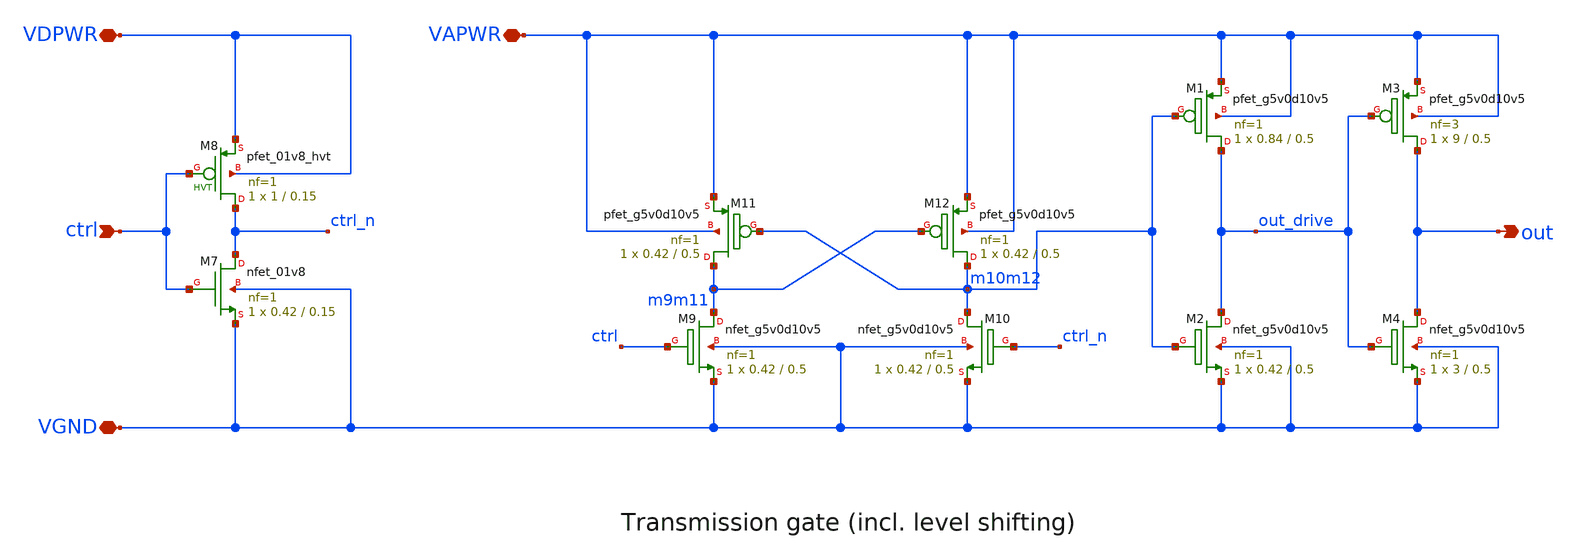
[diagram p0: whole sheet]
** sch_path: xschem/dac_drive.sch
**.subckt dac_drive ctrl VGND VDPWR VAPWR out
*.ipin ctrl
*.iopin VGND
*.iopin VDPWR
*.iopin VAPWR
*.opin out
XM8 ctrl_n ctrl VDPWR VDPWR sky130_fd_pr__pfet_01v8_hvt L=0.15 W=1 nf=1 ad='int((nf+1)/2) * W/nf * 0.29'
+ as='int((nf+2)/2) * W/nf * 0.29' pd='2*int((nf+1)/2) * (W/nf + 0.29)' ps='2*int((nf+2)/2) * (W/nf + 0.29)'
+ nrd='0.29 / W' nrs='0.29 / W' sa=0 sb=0 sd=0 mult=1 m=1
XM7 ctrl_n ctrl VGND VGND sky130_fd_pr__nfet_01v8 L=0.15 W=0.42 nf=1 ad='int((nf+1)/2) * W/nf * 0.29'
+ as='int((nf+2)/2) * W/nf * 0.29' pd='2*int((nf+1)/2) * (W/nf + 0.29)' ps='2*int((nf+2)/2) * (W/nf + 0.29)'
+ nrd='0.29 / W' nrs='0.29 / W' sa=0 sb=0 sd=0 mult=1 m=1
XM11 m9m11 m10m12 VAPWR VAPWR sky130_fd_pr__pfet_g5v0d10v5 L=0.5 W=0.42 nf=1 ad='int((nf+1)/2) * W/nf * 0.29'
+ as='int((nf+2)/2) * W/nf * 0.29' pd='2*int((nf+1)/2) * (W/nf + 0.29)' ps='2*int((nf+2)/2) * (W/nf + 0.29)'
+ nrd='0.29 / W' nrs='0.29 / W' sa=0 sb=0 sd=0 mult=1 m=1
XM9 m9m11 ctrl VGND VGND sky130_fd_pr__nfet_g5v0d10v5 L=0.5 W=0.42 nf=1 ad='int((nf+1)/2) * W/nf * 0.29'
+ as='int((nf+2)/2) * W/nf * 0.29' pd='2*int((nf+1)/2) * (W/nf + 0.29)' ps='2*int((nf+2)/2) * (W/nf + 0.29)'
+ nrd='0.29 / W' nrs='0.29 / W' sa=0 sb=0 sd=0 mult=1 m=1
XM10 m10m12 ctrl_n VGND VGND sky130_fd_pr__nfet_g5v0d10v5 L=0.5 W=0.42 nf=1 ad='int((nf+1)/2) * W/nf * 0.29'
+ as='int((nf+2)/2) * W/nf * 0.29' pd='2*int((nf+1)/2) * (W/nf + 0.29)' ps='2*int((nf+2)/2) * (W/nf + 0.29)'
+ nrd='0.29 / W' nrs='0.29 / W' sa=0 sb=0 sd=0 mult=1 m=1
XM12 m10m12 m9m11 VAPWR VAPWR sky130_fd_pr__pfet_g5v0d10v5 L=0.5 W=0.42 nf=1 ad='int((nf+1)/2) * W/nf * 0.29'
+ as='int((nf+2)/2) * W/nf * 0.29' pd='2*int((nf+1)/2) * (W/nf + 0.29)' ps='2*int((nf+2)/2) * (W/nf + 0.29)'
+ nrd='0.29 / W' nrs='0.29 / W' sa=0 sb=0 sd=0 mult=1 m=1
XM1 out_drive m10m12 VAPWR VAPWR sky130_fd_pr__pfet_g5v0d10v5 L=0.5 W=0.84 nf=1 ad='int((nf+1)/2) * W/nf * 0.29'
+ as='int((nf+2)/2) * W/nf * 0.29' pd='2*int((nf+1)/2) * (W/nf + 0.29)' ps='2*int((nf+2)/2) * (W/nf + 0.29)'
+ nrd='0.29 / W' nrs='0.29 / W' sa=0 sb=0 sd=0 mult=1 m=1
XM2 out_drive m10m12 VGND VGND sky130_fd_pr__nfet_g5v0d10v5 L=0.5 W=0.42 nf=1 ad='int((nf+1)/2) * W/nf * 0.29'
+ as='int((nf+2)/2) * W/nf * 0.29' pd='2*int((nf+1)/2) * (W/nf + 0.29)' ps='2*int((nf+2)/2) * (W/nf + 0.29)'
+ nrd='0.29 / W' nrs='0.29 / W' sa=0 sb=0 sd=0 mult=1 m=1
XM3 out out_drive VAPWR VAPWR sky130_fd_pr__pfet_g5v0d10v5 L=0.5 W=9 nf=3 ad='int((nf+1)/2) * W/nf * 0.29'
+ as='int((nf+2)/2) * W/nf * 0.29' pd='2*int((nf+1)/2) * (W/nf + 0.29)' ps='2*int((nf+2)/2) * (W/nf + 0.29)'
+ nrd='0.29 / W' nrs='0.29 / W' sa=0 sb=0 sd=0 mult=1 m=1
XM4 out out_drive VGND VGND sky130_fd_pr__nfet_g5v0d10v5 L=0.5 W=3 nf=1 ad='int((nf+1)/2) * W/nf * 0.29'
+ as='int((nf+2)/2) * W/nf * 0.29' pd='2*int((nf+1)/2) * (W/nf + 0.29)' ps='2*int((nf+2)/2) * (W/nf + 0.29)'
+ nrd='0.29 / W' nrs='0.29 / W' sa=0 sb=0 sd=0 mult=1 m=1
**.ends
.end
